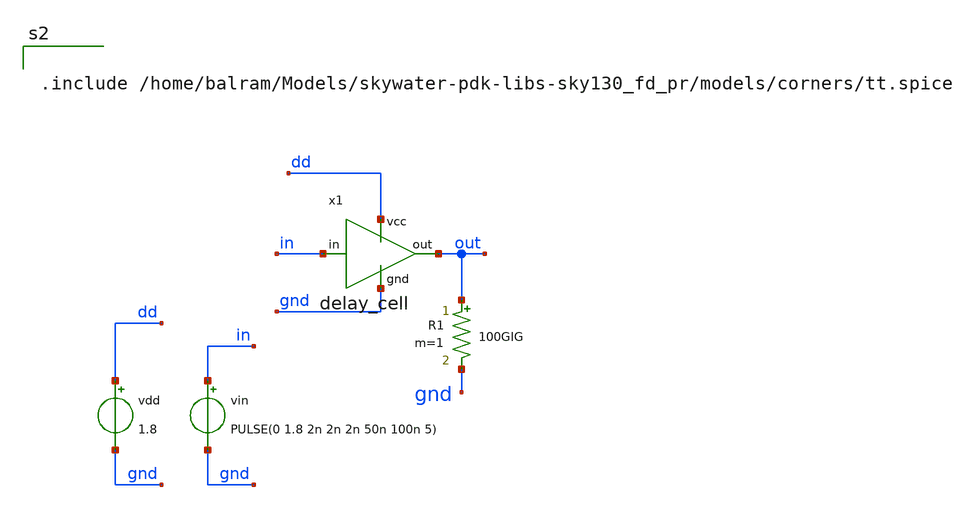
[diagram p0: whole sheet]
** sch_path: Oscillators/Ring-Oscillator/TB__delay_cell.sch
**.subckt TB__delay_cell
x1 dd in out gnd delay_cell
vin in gnd PULSE(0 1.8 2n 2n 2n 50n 100n 5)
vdd dd gnd 1.8
R1 out gnd 100GIG m=1
**** begin user architecture code


.include /home/balram/Models/skywater-pdk-libs-sky130_fd_pr/models/corners/tt.spice


**** end user architecture code
**.ends

* expanding   symbol:  delay_cell.sym # of pins=4
** sym_path: Oscillators/Ring-Oscillator/delay_cell.sym
** sch_path: Oscillators/Ring-Oscillator/delay_cell.sch
.subckt delay_cell vcc in out gnd
*.ipin vcc
*.ipin gnd
*.ipin in
*.opin out
XM1 out in gnd gnd sky130_fd_pr__nfet_01v8_lvt L=0.15 W=0.45 nf=1 ad='int((1 + 1)/2) * 0.45 / 1 * 0.29'
+ as='int((1 + 2)/2) * 0.45 / 1 * 0.29' pd='2*int((1 + 1)/2) * (0.45 / 1 + 0.29)' ps='2*int((1 + 2)/2) * (0.45 / 1 + 0.29)'
+ nrd='0.29 / 0.45 ' nrs='0.29 / 0.45 ' sa=0 sb=0 sd=0 mult=1 m=1
XM10 out in vcc vcc sky130_fd_pr__pfet_01v8_lvt L=0.35 W=0.45 nf=1 ad='int((1 + 1)/2) * 0.45 / 1 * 0.29'
+ as='int((1 + 2)/2) * 0.45 / 1 * 0.29' pd='2*int((1 + 1)/2) * (0.45 / 1 + 0.29)' ps='2*int((1 + 2)/2) * (0.45 / 1 + 0.29)'
+ nrd='0.29 / 0.45 ' nrs='0.29 / 0.45 ' sa=0 sb=0 sd=0 mult=1 m=1
.ends

.end
